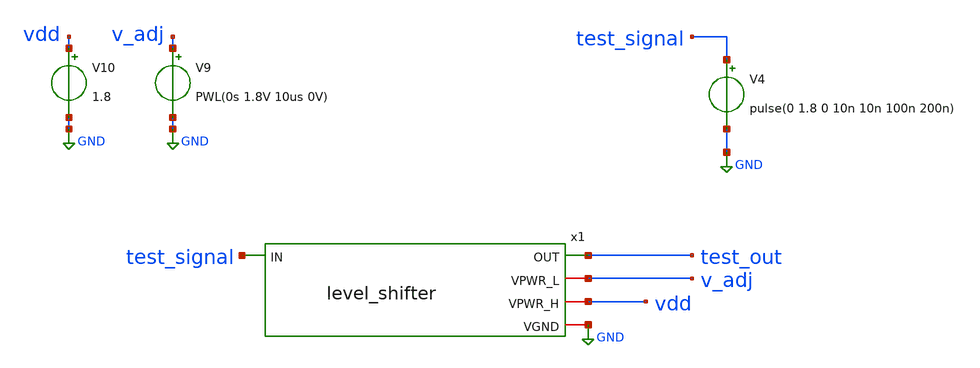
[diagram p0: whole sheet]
** sch_path: xschem/tb_level.sch
**.subckt tb_level
V4 test_signal GND pulse(0 1.8 0 10n 10n 100n 200n)
V9 v_adj GND PWL(0s 1.8V 10us 0V)
V10 vdd GND 1.8
x1 test_out v_adj test_signal vdd GND level_shifter
**** begin user architecture code

** opencircuitdesign pdks install
.lib $::SKYWATER_MODELS/sky130.lib.spice tt




* .options filetype=ascii
.control
tran 1n 10u
write tb_level.raw
.endc
.end


**** end user architecture code
**.ends

* expanding   symbol:  level_shifter.sym # of pins=5
** sym_path: xschem/level_shifter.sym
** sch_path: xschem/level_shifter.sch
.subckt level_shifter OUT VPWR_L IN VPWR_H VGND
*.iopin VGND
*.iopin VPWR_H
*.iopin VPWR_L
*.ipin IN
*.opin OUT
XM1 net2 OUT VPWR_H VPWR_H sky130_fd_pr__pfet_01v8 L=0.15 W=1 nf=1 ad='int((nf+1)/2) * W/nf * 0.29' as='int((nf+2)/2) * W/nf * 0.29'
+ pd='2*int((nf+1)/2) * (W/nf + 0.29)' ps='2*int((nf+2)/2) * (W/nf + 0.29)' nrd='0.29 / W' nrs='0.29 / W'
+ sa=0 sb=0 sd=0 mult=1 m=1
XM2 OUT net2 VPWR_H VPWR_H sky130_fd_pr__pfet_01v8 L=0.15 W=1 nf=1 ad='int((nf+1)/2) * W/nf * 0.29' as='int((nf+2)/2) * W/nf * 0.29'
+ pd='2*int((nf+1)/2) * (W/nf + 0.29)' ps='2*int((nf+2)/2) * (W/nf + 0.29)' nrd='0.29 / W' nrs='0.29 / W'
+ sa=0 sb=0 sd=0 mult=1 m=1
XM3 net2 IN VGND VGND sky130_fd_pr__nfet_01v8 L=0.15 W=1 nf=1 ad='int((nf+1)/2) * W/nf * 0.29' as='int((nf+2)/2) * W/nf * 0.29'
+ pd='2*int((nf+1)/2) * (W/nf + 0.29)' ps='2*int((nf+2)/2) * (W/nf + 0.29)' nrd='0.29 / W' nrs='0.29 / W'
+ sa=0 sb=0 sd=0 mult=1 m=1
XM4 OUT net1 VGND VGND sky130_fd_pr__nfet_01v8 L=0.15 W=1 nf=1 ad='int((nf+1)/2) * W/nf * 0.29' as='int((nf+2)/2) * W/nf * 0.29'
+ pd='2*int((nf+1)/2) * (W/nf + 0.29)' ps='2*int((nf+2)/2) * (W/nf + 0.29)' nrd='0.29 / W' nrs='0.29 / W'
+ sa=0 sb=0 sd=0 mult=1 m=1
XM5 net1 IN VPWR_L VPWR_L sky130_fd_pr__pfet_01v8 L=0.15 W=1 nf=1 ad='int((nf+1)/2) * W/nf * 0.29' as='int((nf+2)/2) * W/nf * 0.29'
+ pd='2*int((nf+1)/2) * (W/nf + 0.29)' ps='2*int((nf+2)/2) * (W/nf + 0.29)' nrd='0.29 / W' nrs='0.29 / W'
+ sa=0 sb=0 sd=0 mult=1 m=1
XM6 net1 IN VGND VGND sky130_fd_pr__nfet_01v8 L=0.15 W=1 nf=1 ad='int((nf+1)/2) * W/nf * 0.29' as='int((nf+2)/2) * W/nf * 0.29'
+ pd='2*int((nf+1)/2) * (W/nf + 0.29)' ps='2*int((nf+2)/2) * (W/nf + 0.29)' nrd='0.29 / W' nrs='0.29 / W'
+ sa=0 sb=0 sd=0 mult=1 m=1
.ends

.GLOBAL GND
.end
